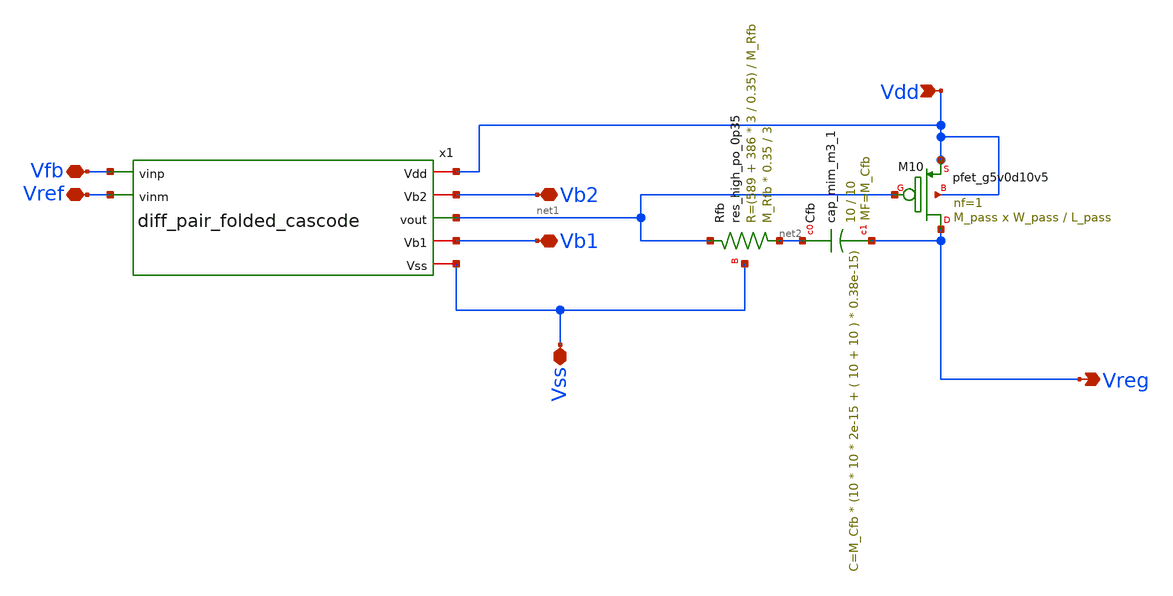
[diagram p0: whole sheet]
** sch_path: xschem/ldo_folded_cascode.sch
**.subckt ldo_folded_cascode Vss Vreg Vref Vdd Vfb Vb2 Vb1
*.iopin Vss
*.opin Vreg
*.iopin Vref
*.ipin Vdd
*.iopin Vfb
*.iopin Vb2
*.iopin Vb1
XM10 Vreg net1 Vdd Vdd sky130_fd_pr__pfet_g5v0d10v5 L=L_pass W=W_pass nf=1 ad='int((nf+1)/2) * W/nf * 0.29'
+ as='int((nf+2)/2) * W/nf * 0.29' pd='2*int((nf+1)/2) * (W/nf + 0.29)' ps='2*int((nf+2)/2) * (W/nf + 0.29)'
+ nrd='0.29 / W' nrs='0.29 / W' sa=0 sb=0 sd=0 mult=M_pass m=M_pass
x1 Vdd Vb2 Vfb Vref net1 Vb1 Vss diff_pair_folded_cascode
XCfb net2 Vreg sky130_fd_pr__cap_mim_m3_1 W=10 L=10 MF=M_Cfb m=M_Cfb
XRfb net2 net1 Vss sky130_fd_pr__res_high_po_0p35 L=3 mult=M_Rfb m=M_Rfb
**.ends

* expanding   symbol:  diff_pair_folded_cascode.sym # of pins=7
** sym_path: xschem/diff_pair_folded_cascode.sym
** sch_path: xschem/diff_pair_folded_cascode.sch
.subckt diff_pair_folded_cascode Vdd Vb2 vinp vinm vout Vb1 Vss
*.iopin Vdd
*.ipin vinm
*.ipin vinp
*.iopin Vb1
*.iopin Vss
*.iopin Vb2
*.opin vout
XM1 net2 vinp net4 Vss sky130_fd_pr__nfet_g5v0d10v5 L=L_M1 W=W_M1 nf=1 ad='int((nf+1)/2) * W/nf * 0.29'
+ as='int((nf+2)/2) * W/nf * 0.29' pd='2*int((nf+1)/2) * (W/nf + 0.29)' ps='2*int((nf+2)/2) * (W/nf + 0.29)'
+ nrd='0.29 / W' nrs='0.29 / W' sa=0 sb=0 sd=0 mult=1 m=1
XM2 net3 vinm net4 Vss sky130_fd_pr__nfet_g5v0d10v5 L=L_M2 W=W_M2 nf=1 ad='int((nf+1)/2) * W/nf * 0.29'
+ as='int((nf+2)/2) * W/nf * 0.29' pd='2*int((nf+1)/2) * (W/nf + 0.29)' ps='2*int((nf+2)/2) * (W/nf + 0.29)'
+ nrd='0.29 / W' nrs='0.29 / W' sa=0 sb=0 sd=0 mult=1 m=1
XM4 net3 net1 Vdd Vdd sky130_fd_pr__pfet_g5v0d10v5 L=L_M4 W=W_M4 nf=1 ad='int((nf+1)/2) * W/nf * 0.29'
+ as='int((nf+2)/2) * W/nf * 0.29' pd='2*int((nf+1)/2) * (W/nf + 0.29)' ps='2*int((nf+2)/2) * (W/nf + 0.29)'
+ nrd='0.29 / W' nrs='0.29 / W' sa=0 sb=0 sd=0 mult=1 m=1
XM3 net2 net1 Vdd Vdd sky130_fd_pr__pfet_g5v0d10v5 L=L_M3 W=W_M3 nf=1 ad='int((nf+1)/2) * W/nf * 0.29'
+ as='int((nf+2)/2) * W/nf * 0.29' pd='2*int((nf+1)/2) * (W/nf + 0.29)' ps='2*int((nf+2)/2) * (W/nf + 0.29)'
+ nrd='0.29 / W' nrs='0.29 / W' sa=0 sb=0 sd=0 mult=1 m=1
XM9 net4 Vb1 Vss Vss sky130_fd_pr__nfet_g5v0d10v5 L=L_M9 W=W_M9 nf=1 ad='int((nf+1)/2) * W/nf * 0.29'
+ as='int((nf+2)/2) * W/nf * 0.29' pd='2*int((nf+1)/2) * (W/nf + 0.29)' ps='2*int((nf+2)/2) * (W/nf + 0.29)'
+ nrd='0.29 / W' nrs='0.29 / W' sa=0 sb=0 sd=0 mult=1 m=1
XM6 vout Vb2 net3 Vdd sky130_fd_pr__pfet_g5v0d10v5 L=L_M6 W=W_M6 nf=1 ad='int((nf+1)/2) * W/nf * 0.29'
+ as='int((nf+2)/2) * W/nf * 0.29' pd='2*int((nf+1)/2) * (W/nf + 0.29)' ps='2*int((nf+2)/2) * (W/nf + 0.29)'
+ nrd='0.29 / W' nrs='0.29 / W' sa=0 sb=0 sd=0 mult=1 m=1
XM5 net1 Vb2 net2 Vdd sky130_fd_pr__pfet_g5v0d10v5 L=L_M5 W=W_M5 nf=1 ad='int((nf+1)/2) * W/nf * 0.29'
+ as='int((nf+2)/2) * W/nf * 0.29' pd='2*int((nf+1)/2) * (W/nf + 0.29)' ps='2*int((nf+2)/2) * (W/nf + 0.29)'
+ nrd='0.29 / W' nrs='0.29 / W' sa=0 sb=0 sd=0 mult=1 m=1
XM7 net1 Vb1 Vss Vss sky130_fd_pr__nfet_g5v0d10v5 L=L_M7 W=W_M7 nf=1 ad='int((nf+1)/2) * W/nf * 0.29'
+ as='int((nf+2)/2) * W/nf * 0.29' pd='2*int((nf+1)/2) * (W/nf + 0.29)' ps='2*int((nf+2)/2) * (W/nf + 0.29)'
+ nrd='0.29 / W' nrs='0.29 / W' sa=0 sb=0 sd=0 mult=1 m=1
XM8 vout Vb1 Vss Vss sky130_fd_pr__nfet_g5v0d10v5 L=L_M8 W=W_M8 nf=1 ad='int((nf+1)/2) * W/nf * 0.29'
+ as='int((nf+2)/2) * W/nf * 0.29' pd='2*int((nf+1)/2) * (W/nf + 0.29)' ps='2*int((nf+2)/2) * (W/nf + 0.29)'
+ nrd='0.29 / W' nrs='0.29 / W' sa=0 sb=0 sd=0 mult=1 m=1
.ends

.end
